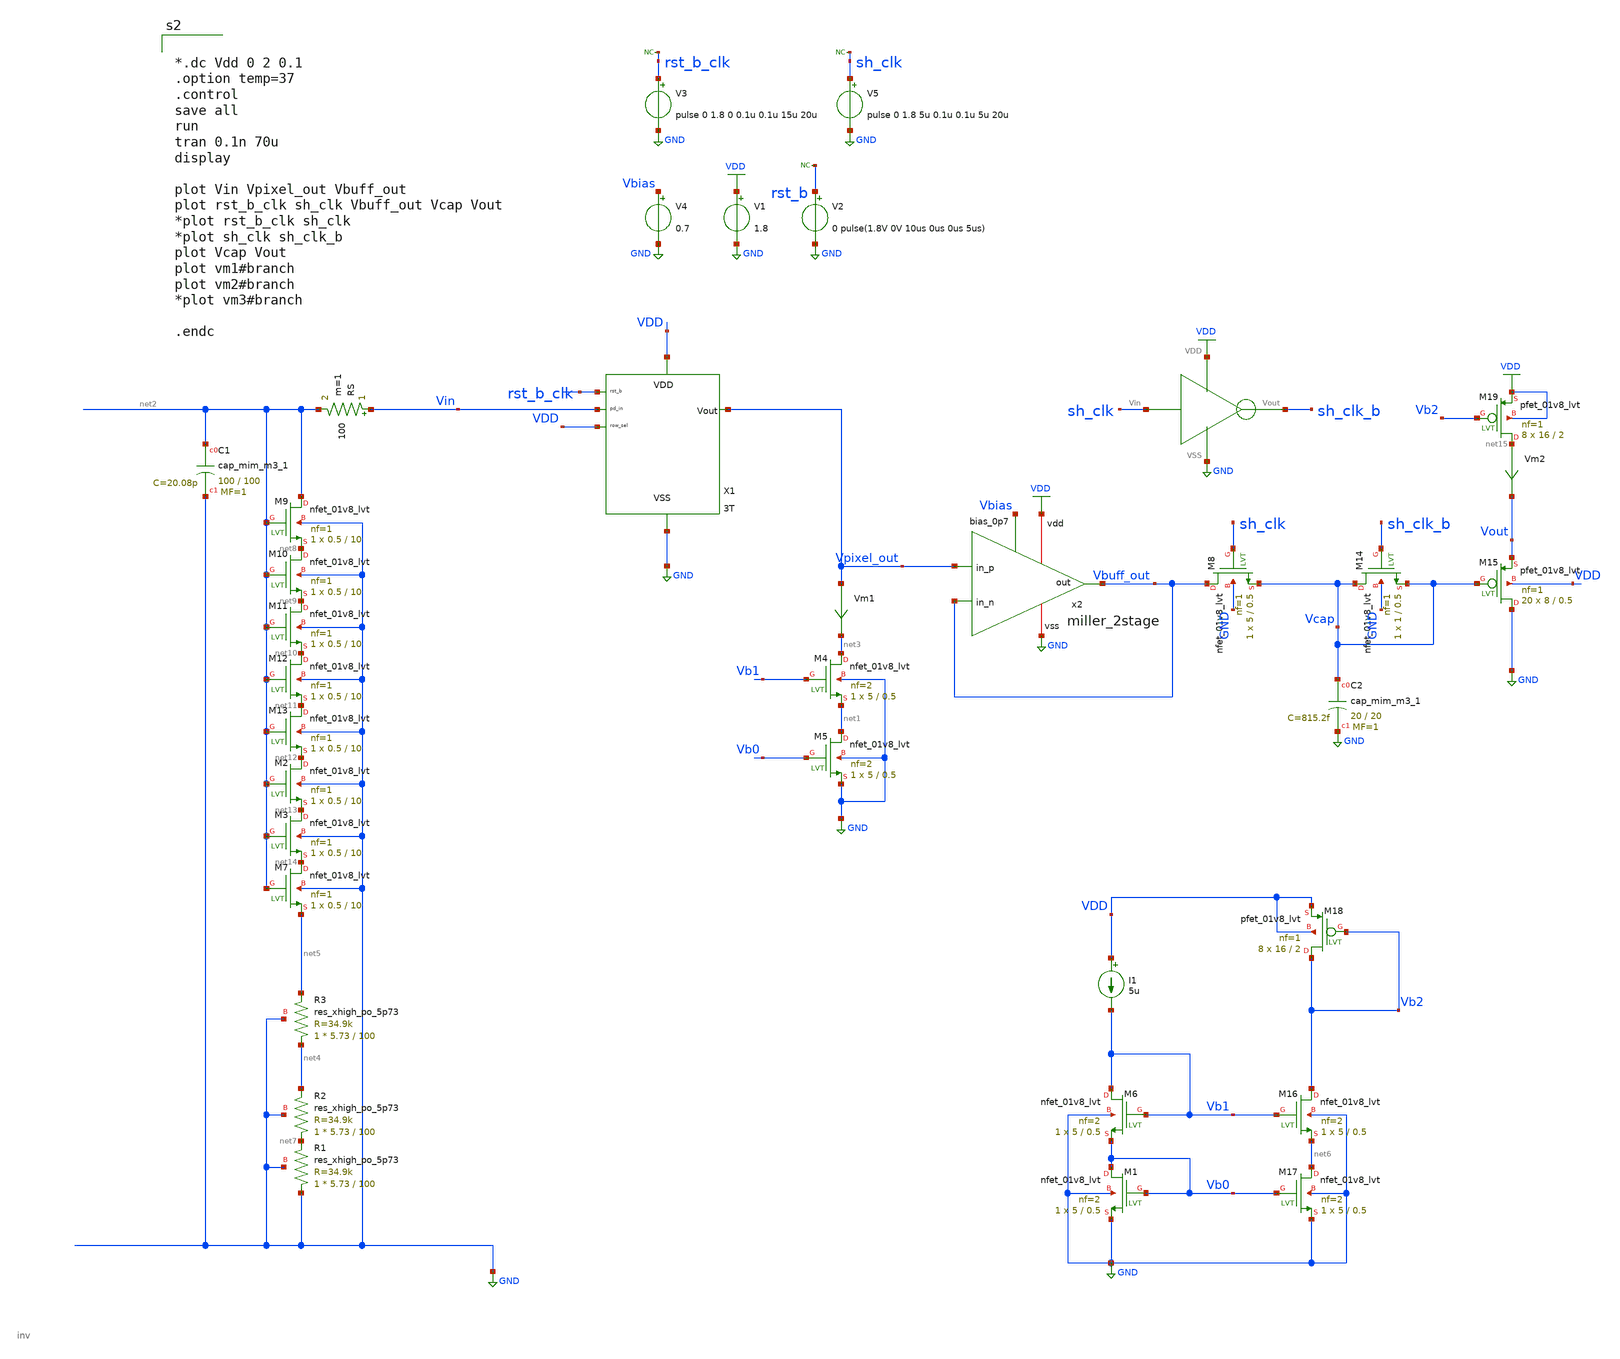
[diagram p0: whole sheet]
** sch_path: xschem/cmos_imager/tb_pixel_real_rc_buffer_sh.sch
**.subckt tb_pixel_real_rc_buffer_sh
XM4 net3 Vb1 net1 GND sky130_fd_pr__nfet_01v8_lvt L=0.5 W=5 nf=2 ad='int((nf+1)/2) * W/nf * 0.29' as='int((nf+2)/2) * W/nf * 0.29'
+ pd='2*int((nf+1)/2) * (W/nf + 0.29)' ps='2*int((nf+2)/2) * (W/nf + 0.29)' nrd='0.29 / W' nrs='0.29 / W'
+ sa=0 sb=0 sd=0 mult=1 m=1
XM5 net1 Vb0 GND GND sky130_fd_pr__nfet_01v8_lvt L=0.5 W=5 nf=2 ad='int((nf+1)/2) * W/nf * 0.29' as='int((nf+2)/2) * W/nf * 0.29'
+ pd='2*int((nf+1)/2) * (W/nf + 0.29)' ps='2*int((nf+2)/2) * (W/nf + 0.29)' nrd='0.29 / W' nrs='0.29 / W'
+ sa=0 sb=0 sd=0 mult=1 m=1
RS Vin net2 100 m=1
XM6 Vb1 Vb1 Vb0 GND sky130_fd_pr__nfet_01v8_lvt L=0.5 W=5 nf=2 ad='int((nf+1)/2) * W/nf * 0.29' as='int((nf+2)/2) * W/nf * 0.29'
+ pd='2*int((nf+1)/2) * (W/nf + 0.29)' ps='2*int((nf+2)/2) * (W/nf + 0.29)' nrd='0.29 / W' nrs='0.29 / W'
+ sa=0 sb=0 sd=0 mult=1 m=1
XM1 Vb0 Vb0 GND GND sky130_fd_pr__nfet_01v8_lvt L=0.5 W=5 nf=2 ad='int((nf+1)/2) * W/nf * 0.29' as='int((nf+2)/2) * W/nf * 0.29'
+ pd='2*int((nf+1)/2) * (W/nf + 0.29)' ps='2*int((nf+2)/2) * (W/nf + 0.29)' nrd='0.29 / W' nrs='0.29 / W'
+ sa=0 sb=0 sd=0 mult=1 m=1
I1 VDD Vb1 5u
V1 VDD GND 1.8
Vm1 Vpixel_out net3 0
.save i(vm1)
V2 rst_b GND 0 pulse(1.8V 0V 10us 0us 0us 5us)
X1 VDD Vin rst_b_clk VDD GND Vpixel_out 3T
XC1 net2 GND sky130_fd_pr__cap_mim_m3_1 W=100 L=100 MF=1 m=1
XR1 GND net7 GND sky130_fd_pr__res_xhigh_po_5p73 L=100 mult=1 m=1
XR2 net7 net4 GND sky130_fd_pr__res_xhigh_po_5p73 L=100 mult=1 m=1
XM9 net2 net2 net8 GND sky130_fd_pr__nfet_01v8_lvt L=10 W=0.5 nf=1 ad='int((nf+1)/2) * W/nf * 0.29' as='int((nf+2)/2) * W/nf * 0.29'
+ pd='2*int((nf+1)/2) * (W/nf + 0.29)' ps='2*int((nf+2)/2) * (W/nf + 0.29)' nrd='0.29 / W' nrs='0.29 / W'
+ sa=0 sb=0 sd=0 mult=1 m=1
XM10 net8 net2 net9 GND sky130_fd_pr__nfet_01v8_lvt L=10 W=0.5 nf=1 ad='int((nf+1)/2) * W/nf * 0.29'
+ as='int((nf+2)/2) * W/nf * 0.29' pd='2*int((nf+1)/2) * (W/nf + 0.29)' ps='2*int((nf+2)/2) * (W/nf + 0.29)'
+ nrd='0.29 / W' nrs='0.29 / W' sa=0 sb=0 sd=0 mult=1 m=1
XM11 net9 net2 net10 GND sky130_fd_pr__nfet_01v8_lvt L=10 W=0.5 nf=1 ad='int((nf+1)/2) * W/nf * 0.29'
+ as='int((nf+2)/2) * W/nf * 0.29' pd='2*int((nf+1)/2) * (W/nf + 0.29)' ps='2*int((nf+2)/2) * (W/nf + 0.29)'
+ nrd='0.29 / W' nrs='0.29 / W' sa=0 sb=0 sd=0 mult=1 m=1
XM12 net10 net2 net11 GND sky130_fd_pr__nfet_01v8_lvt L=10 W=0.5 nf=1 ad='int((nf+1)/2) * W/nf * 0.29'
+ as='int((nf+2)/2) * W/nf * 0.29' pd='2*int((nf+1)/2) * (W/nf + 0.29)' ps='2*int((nf+2)/2) * (W/nf + 0.29)'
+ nrd='0.29 / W' nrs='0.29 / W' sa=0 sb=0 sd=0 mult=1 m=1
XM13 net11 net2 net12 GND sky130_fd_pr__nfet_01v8_lvt L=10 W=0.5 nf=1 ad='int((nf+1)/2) * W/nf * 0.29'
+ as='int((nf+2)/2) * W/nf * 0.29' pd='2*int((nf+1)/2) * (W/nf + 0.29)' ps='2*int((nf+2)/2) * (W/nf + 0.29)'
+ nrd='0.29 / W' nrs='0.29 / W' sa=0 sb=0 sd=0 mult=1 m=1
XM2 net12 net2 net13 GND sky130_fd_pr__nfet_01v8_lvt L=10 W=0.5 nf=1 ad='int((nf+1)/2) * W/nf * 0.29'
+ as='int((nf+2)/2) * W/nf * 0.29' pd='2*int((nf+1)/2) * (W/nf + 0.29)' ps='2*int((nf+2)/2) * (W/nf + 0.29)'
+ nrd='0.29 / W' nrs='0.29 / W' sa=0 sb=0 sd=0 mult=1 m=1
XM3 net13 net2 net14 GND sky130_fd_pr__nfet_01v8_lvt L=10 W=0.5 nf=1 ad='int((nf+1)/2) * W/nf * 0.29'
+ as='int((nf+2)/2) * W/nf * 0.29' pd='2*int((nf+1)/2) * (W/nf + 0.29)' ps='2*int((nf+2)/2) * (W/nf + 0.29)'
+ nrd='0.29 / W' nrs='0.29 / W' sa=0 sb=0 sd=0 mult=1 m=1
XM7 net14 net2 net5 GND sky130_fd_pr__nfet_01v8_lvt L=10 W=0.5 nf=1 ad='int((nf+1)/2) * W/nf * 0.29'
+ as='int((nf+2)/2) * W/nf * 0.29' pd='2*int((nf+1)/2) * (W/nf + 0.29)' ps='2*int((nf+2)/2) * (W/nf + 0.29)'
+ nrd='0.29 / W' nrs='0.29 / W' sa=0 sb=0 sd=0 mult=1 m=1
V3 rst_b_clk GND pulse 0 1.8 0 0.1u 0.1u 15u 20u
* noconn rst_b_clk
* noconn rst_b
XR3 net4 net5 GND sky130_fd_pr__res_xhigh_po_5p73 L=100 mult=1 m=1
x2 VDD Vbuff_out Vpixel_out Vbuff_out Vbias GND miller_2stage
V4 Vbias GND 0.7
XM8 Vbuff_out sh_clk Vcap GND sky130_fd_pr__nfet_01v8_lvt L=0.5 W=5 nf=1 ad='int((nf+1)/2) * W/nf * 0.29'
+ as='int((nf+2)/2) * W/nf * 0.29' pd='2*int((nf+1)/2) * (W/nf + 0.29)' ps='2*int((nf+2)/2) * (W/nf + 0.29)'
+ nrd='0.29 / W' nrs='0.29 / W' sa=0 sb=0 sd=0 mult=1 m=1
XM14 Vcap sh_clk_b Vcap GND sky130_fd_pr__nfet_01v8_lvt L=0.5 W=1 nf=1 ad='int((nf+1)/2) * W/nf * 0.29'
+ as='int((nf+2)/2) * W/nf * 0.29' pd='2*int((nf+1)/2) * (W/nf + 0.29)' ps='2*int((nf+2)/2) * (W/nf + 0.29)'
+ nrd='0.29 / W' nrs='0.29 / W' sa=0 sb=0 sd=0 mult=1 m=1
XC2 Vcap GND sky130_fd_pr__cap_mim_m3_1 W=20 L=20 MF=1 m=1
V5 sh_clk GND pulse 0 1.8 5u 0.1u 0.1u 5u 20u
* noconn sh_clk
X3 sh_clk sh_clk_b GND VDD inv
XM15 GND Vcap Vout VDD sky130_fd_pr__pfet_01v8_lvt L=0.5 W=8 nf=1 ad='int((nf+1)/2) * W/nf * 0.29' as='int((nf+2)/2) * W/nf * 0.29'
+ pd='2*int((nf+1)/2) * (W/nf + 0.29)' ps='2*int((nf+2)/2) * (W/nf + 0.29)' nrd='0.29 / W' nrs='0.29 / W'
+ sa=0 sb=0 sd=0 mult=20 m=20
XM16 Vb2 Vb1 net6 GND sky130_fd_pr__nfet_01v8_lvt L=0.5 W=5 nf=2 ad='int((nf+1)/2) * W/nf * 0.29' as='int((nf+2)/2) * W/nf * 0.29'
+ pd='2*int((nf+1)/2) * (W/nf + 0.29)' ps='2*int((nf+2)/2) * (W/nf + 0.29)' nrd='0.29 / W' nrs='0.29 / W'
+ sa=0 sb=0 sd=0 mult=1 m=1
XM17 net6 Vb0 GND GND sky130_fd_pr__nfet_01v8_lvt L=0.5 W=5 nf=2 ad='int((nf+1)/2) * W/nf * 0.29' as='int((nf+2)/2) * W/nf * 0.29'
+ pd='2*int((nf+1)/2) * (W/nf + 0.29)' ps='2*int((nf+2)/2) * (W/nf + 0.29)' nrd='0.29 / W' nrs='0.29 / W'
+ sa=0 sb=0 sd=0 mult=1 m=1
XM18 Vb2 Vb2 VDD VDD sky130_fd_pr__pfet_01v8_lvt L=2 W=16 nf=1 ad='int((nf+1)/2) * W/nf * 0.29' as='int((nf+2)/2) * W/nf * 0.29'
+ pd='2*int((nf+1)/2) * (W/nf + 0.29)' ps='2*int((nf+2)/2) * (W/nf + 0.29)' nrd='0.29 / W' nrs='0.29 / W'
+ sa=0 sb=0 sd=0 mult=8 m=8
XM19 net15 Vb2 VDD VDD sky130_fd_pr__pfet_01v8_lvt L=2 W=16 nf=1 ad='int((nf+1)/2) * W/nf * 0.29' as='int((nf+2)/2) * W/nf * 0.29'
+ pd='2*int((nf+1)/2) * (W/nf + 0.29)' ps='2*int((nf+2)/2) * (W/nf + 0.29)' nrd='0.29 / W' nrs='0.29 / W'
+ sa=0 sb=0 sd=0 mult=8 m=8
Vm2 net15 Vout 0
.save i(vm2)
**** begin user architecture code

** opencircuitdesign pdks install
.lib $::SKYWATER_MODELS/sky130.lib.spice tt




*.dc Vdd 0 2 0.1
.option temp=37
.control
save all
run
tran 0.1n 70u
display

plot Vin Vpixel_out Vbuff_out
plot rst_b_clk sh_clk Vbuff_out Vcap Vout
*plot rst_b_clk sh_clk
*plot sh_clk sh_clk_b
plot Vcap Vout
plot vm1#branch
plot vm2#branch
*plot vm3#branch

.endc


**** end user architecture code
**.ends
.GLOBAL GND
.GLOBAL VDD
.end
